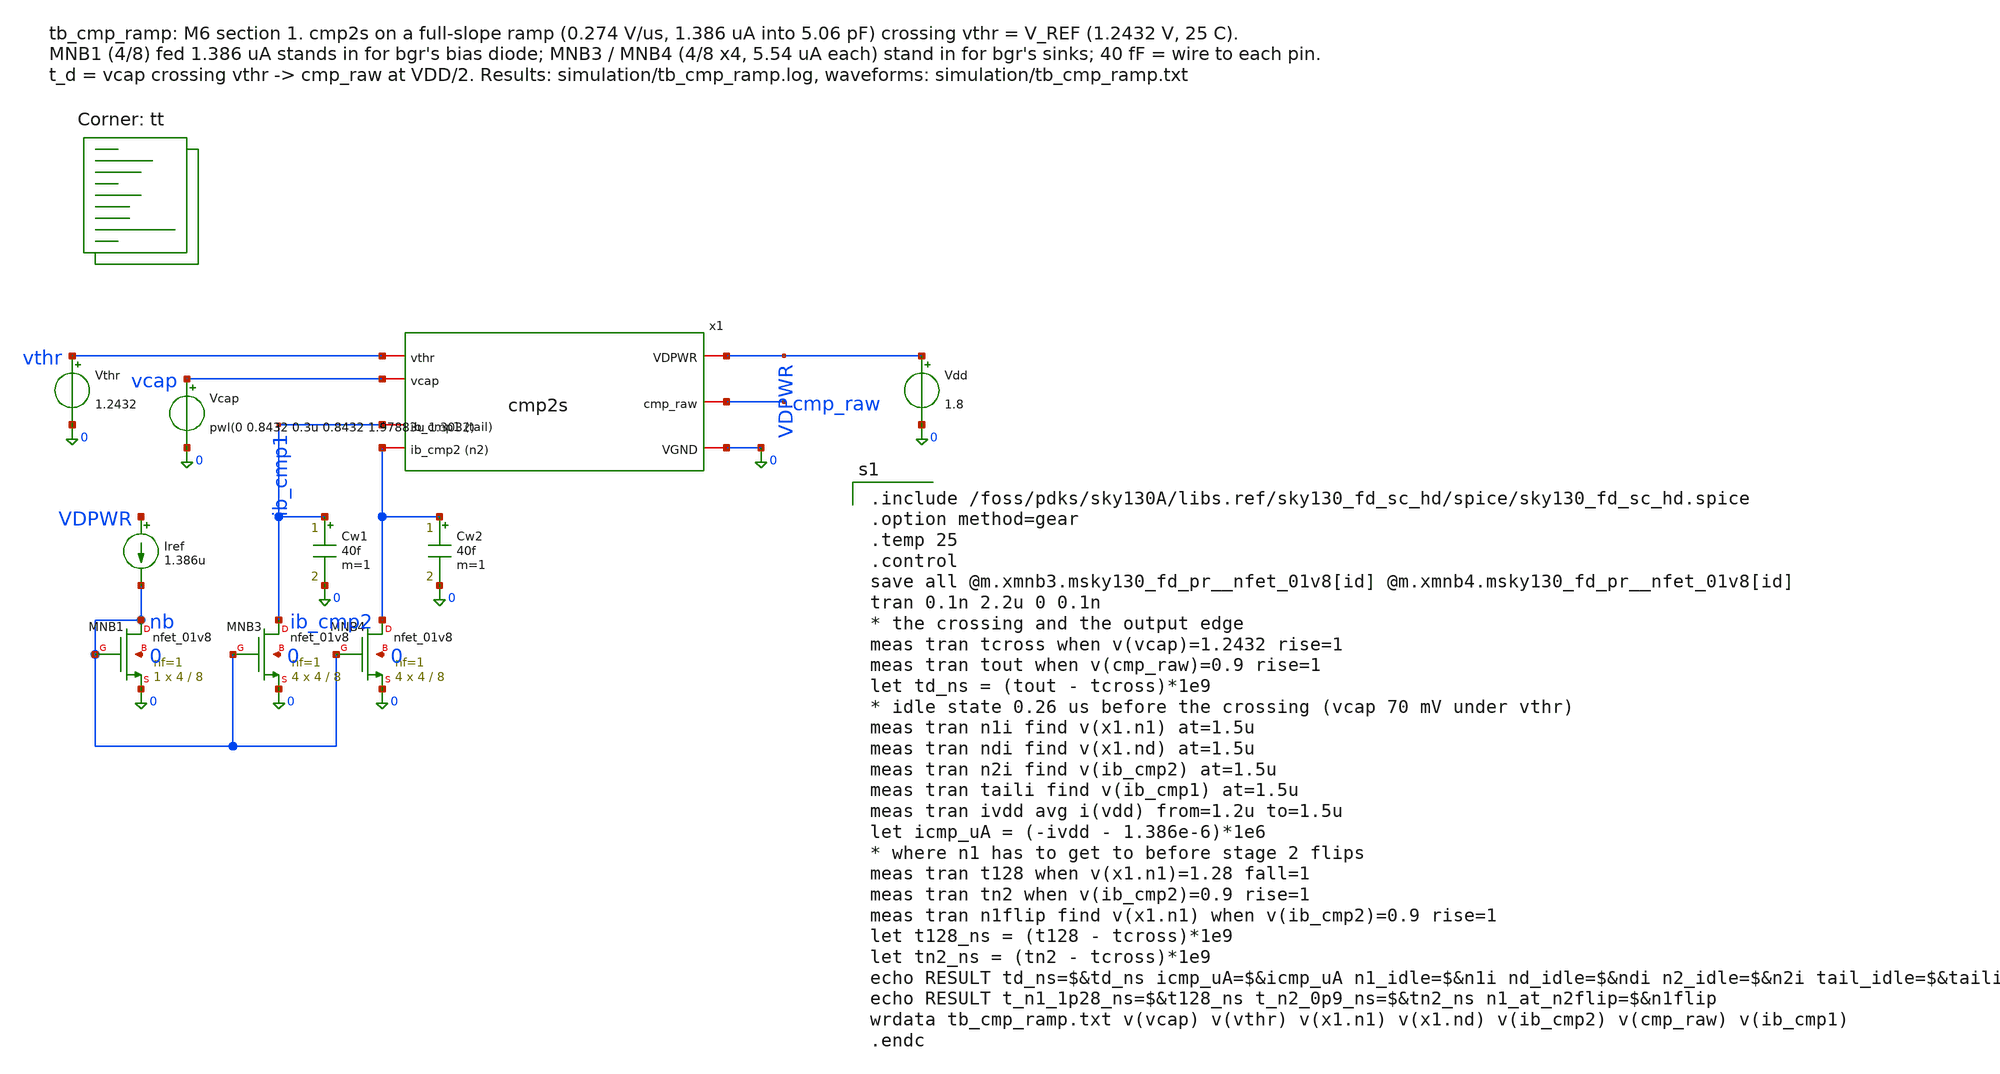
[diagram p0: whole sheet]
** sch_path: xschem/tb_cmp_ramp.sch
**.subckt tb_cmp_ramp
x1 vthr vcap ib_cmp1 ib_cmp2 VDPWR cmp_raw 0 cmp2s
Vthr vthr 0 1.2432
Vcap vcap 0 pwl(0 0.8432 0.3u 0.8432 1.97883u 1.3032)
Vdd VDPWR 0 1.8
Iref VDPWR nb 1.386u
Cw1 ib_cmp1 0 40f m=1
Cw2 ib_cmp2 0 40f m=1
XMNB1 nb nb 0 0 sky130_fd_pr__nfet_01v8 L=8 W=4 nf=1 ad='int((1 + 1)/2) * 4 / 1 * 0.29' as='int((1 + 2)/2) * 4 / 1 * 0.29'
+ pd='2*int((1 + 1)/2) * (4 / 1 + 0.29)' ps='2*int((1 + 2)/2) * (4 / 1 + 0.29)' nrd='0.29 / 4 ' nrs='0.29 / 4 '
+ sa=0 sb=0 sd=0 mult=1 m=1
XMNB3 ib_cmp1 nb 0 0 sky130_fd_pr__nfet_01v8 L=8 W=4 nf=1 ad='int((1 + 1)/2) * 4 / 1 * 0.29' as='int((1 + 2)/2) * 4 / 1 * 0.29'
+ pd='2*int((1 + 1)/2) * (4 / 1 + 0.29)' ps='2*int((1 + 2)/2) * (4 / 1 + 0.29)' nrd='0.29 / 4 ' nrs='0.29 / 4 '
+ sa=0 sb=0 sd=0 mult=4 m=4
XMNB4 ib_cmp2 nb 0 0 sky130_fd_pr__nfet_01v8 L=8 W=4 nf=1 ad='int((1 + 1)/2) * 4 / 1 * 0.29' as='int((1 + 2)/2) * 4 / 1 * 0.29'
+ pd='2*int((1 + 1)/2) * (4 / 1 + 0.29)' ps='2*int((1 + 2)/2) * (4 / 1 + 0.29)' nrd='0.29 / 4 ' nrs='0.29 / 4 '
+ sa=0 sb=0 sd=0 mult=4 m=4
**** begin user architecture code
.lib $::SKYWATER_MODELS/sky130.lib.spice tt

.include /foss/pdks/sky130A/libs.ref/sky130_fd_sc_hd/spice/sky130_fd_sc_hd.spice
.option method=gear
.temp 25
.control
save all @m.xmnb3.msky130_fd_pr__nfet_01v8[id] @m.xmnb4.msky130_fd_pr__nfet_01v8[id]
tran 0.1n 2.2u 0 0.1n
* the crossing and the output edge
meas tran tcross when v(vcap)=1.2432 rise=1
meas tran tout when v(cmp_raw)=0.9 rise=1
let td_ns = (tout - tcross)*1e9
* idle state 0.26 us before the crossing (vcap 70 mV under vthr)
meas tran n1i find v(x1.n1) at=1.5u
meas tran ndi find v(x1.nd) at=1.5u
meas tran n2i find v(ib_cmp2) at=1.5u
meas tran taili find v(ib_cmp1) at=1.5u
meas tran ivdd avg i(vdd) from=1.2u to=1.5u
let icmp_uA = (-ivdd - 1.386e-6)*1e6
* where n1 has to get to before stage 2 flips
meas tran t128 when v(x1.n1)=1.28 fall=1
meas tran tn2 when v(ib_cmp2)=0.9 rise=1
meas tran n1flip find v(x1.n1) when v(ib_cmp2)=0.9 rise=1
let t128_ns = (t128 - tcross)*1e9
let tn2_ns = (tn2 - tcross)*1e9
echo RESULT td_ns=$&td_ns icmp_uA=$&icmp_uA n1_idle=$&n1i nd_idle=$&ndi n2_idle=$&n2i
+ tail_idle=$&taili
echo RESULT t_n1_1p28_ns=$&t128_ns t_n2_0p9_ns=$&tn2_ns n1_at_n2flip=$&n1flip
wrdata tb_cmp_ramp.txt v(vcap) v(vthr) v(x1.n1) v(x1.nd) v(ib_cmp2) v(cmp_raw) v(ib_cmp1)
.endc

**** end user architecture code
**.ends

* expanding   symbol:  cmp2s.sym # of pins=7
** sym_path: xschem/cmp2s.sym
** sch_path: xschem/cmp2s.sch
.subckt cmp2s vthr vcap ib_cmp1 ib_cmp2 VDPWR cmp_raw VGND
*.iopin VDPWR
*.iopin VGND
*.ipin vthr
*.ipin vcap
*.iopin ib_cmp1
*.iopin ib_cmp2
*.opin cmp_raw
XM2a nd nd VDPWR VDPWR sky130_fd_pr__pfet_01v8_lvt L=4 W=4 nf=1 ad='int((1 + 1)/2) * 4 / 1 * 0.29' as='int((1 + 2)/2) * 4 / 1 * 0.29'
+ pd='2*int((1 + 1)/2) * (4 / 1 + 0.29)' ps='2*int((1 + 2)/2) * (4 / 1 + 0.29)' nrd='0.29 / 4 ' nrs='0.29 / 4 '
+ sa=0 sb=0 sd=0 mult=8 m=8
XM2b n1 nd VDPWR VDPWR sky130_fd_pr__pfet_01v8_lvt L=4 W=4 nf=1 ad='int((1 + 1)/2) * 4 / 1 * 0.29' as='int((1 + 2)/2) * 4 / 1 * 0.29'
+ pd='2*int((1 + 1)/2) * (4 / 1 + 0.29)' ps='2*int((1 + 2)/2) * (4 / 1 + 0.29)' nrd='0.29 / 4 ' nrs='0.29 / 4 '
+ sa=0 sb=0 sd=0 mult=8 m=8
XM1a nd vthr ib_cmp1 VGND sky130_fd_pr__nfet_01v8_lvt L=1.75 W=10 nf=1 ad='int((1 + 1)/2) * 10 / 1 * 0.29'
+ as='int((1 + 2)/2) * 10 / 1 * 0.29' pd='2*int((1 + 1)/2) * (10 / 1 + 0.29)' ps='2*int((1 + 2)/2) * (10 / 1 + 0.29)'
+ nrd='0.29 / 10 ' nrs='0.29 / 10 ' sa=0 sb=0 sd=0 mult=6 m=6
XM1b n1 vcap ib_cmp1 VGND sky130_fd_pr__nfet_01v8_lvt L=1.75 W=10 nf=1 ad='int((1 + 1)/2) * 10 / 1 * 0.29'
+ as='int((1 + 2)/2) * 10 / 1 * 0.29' pd='2*int((1 + 1)/2) * (10 / 1 + 0.29)' ps='2*int((1 + 2)/2) * (10 / 1 + 0.29)'
+ nrd='0.29 / 10 ' nrs='0.29 / 10 ' sa=0 sb=0 sd=0 mult=6 m=6
XM3 ib_cmp2 n1 VDPWR VDPWR sky130_fd_pr__pfet_01v8_lvt L=1 W=4 nf=1 ad='int((1 + 1)/2) * 4 / 1 * 0.29'
+ as='int((1 + 2)/2) * 4 / 1 * 0.29' pd='2*int((1 + 1)/2) * (4 / 1 + 0.29)' ps='2*int((1 + 2)/2) * (4 / 1 + 0.29)'
+ nrd='0.29 / 4 ' nrs='0.29 / 4 ' sa=0 sb=0 sd=0 mult=3 m=3
XMIP x ib_cmp2 VDPWR VDPWR sky130_fd_pr__pfet_01v8 L=1 W=0.42 nf=1 ad='int((1 + 1)/2) * 0.42 / 1 * 0.29'
+ as='int((1 + 2)/2) * 0.42 / 1 * 0.29' pd='2*int((1 + 1)/2) * (0.42 / 1 + 0.29)' ps='2*int((1 + 2)/2) * (0.42 / 1 + 0.29)'
+ nrd='0.29 / 0.42 ' nrs='0.29 / 0.42 ' sa=0 sb=0 sd=0 mult=1 m=1
XMIN x ib_cmp2 VGND VGND sky130_fd_pr__nfet_01v8 L=0.15 W=2 nf=1 ad='int((1 + 1)/2) * 2 / 1 * 0.29' as='int((1 + 2)/2) * 2 / 1 * 0.29'
+ pd='2*int((1 + 1)/2) * (2 / 1 + 0.29)' ps='2*int((1 + 2)/2) * (2 / 1 + 0.29)' nrd='0.29 / 2 ' nrs='0.29 / 2 '
+ sa=0 sb=0 sd=0 mult=1 m=1
xinv x VGND VGND VDPWR VDPWR cmp_raw sky130_fd_sc_hd__inv_1
.ends

.end
